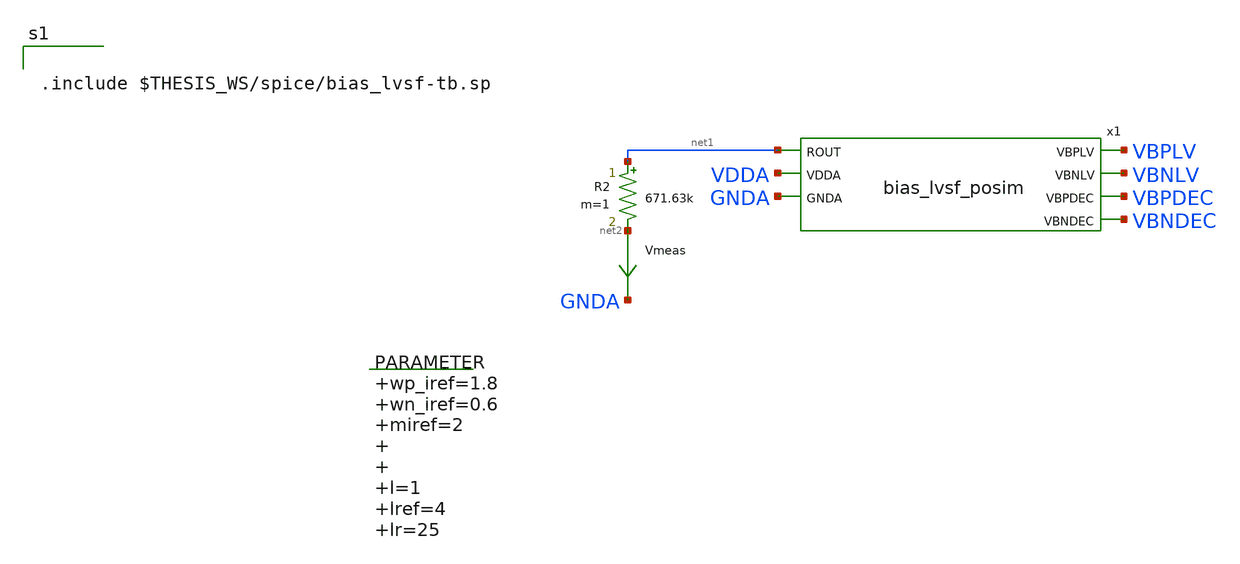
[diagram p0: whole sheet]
** sch_path: xschem/bias_lvsf-tb.sch
.lib $::SKYWATER_MODELS/sky130.lib.spice tt
.include $::SKYWATER_STDCELLS/sky130_fd_sc_hd.spice

**.subckt bias_lvsf-tb
.param wp_iref=1.8 wn_iref=0.6 miref=2 l=1 lref=4 lr=25
R2 net1 net2 671.63k m=1
Vmeas net2 GNDA 0
.save i(vmeas)
x1 net1 VBPLV VBNLV VBPDEC VBNDEC VDDA GNDA bias_lvsf_posim
**** begin user architecture code


.include $THESIS_WS/spice/bias_lvsf-tb.sp

**** end user architecture code
**.ends
.end
